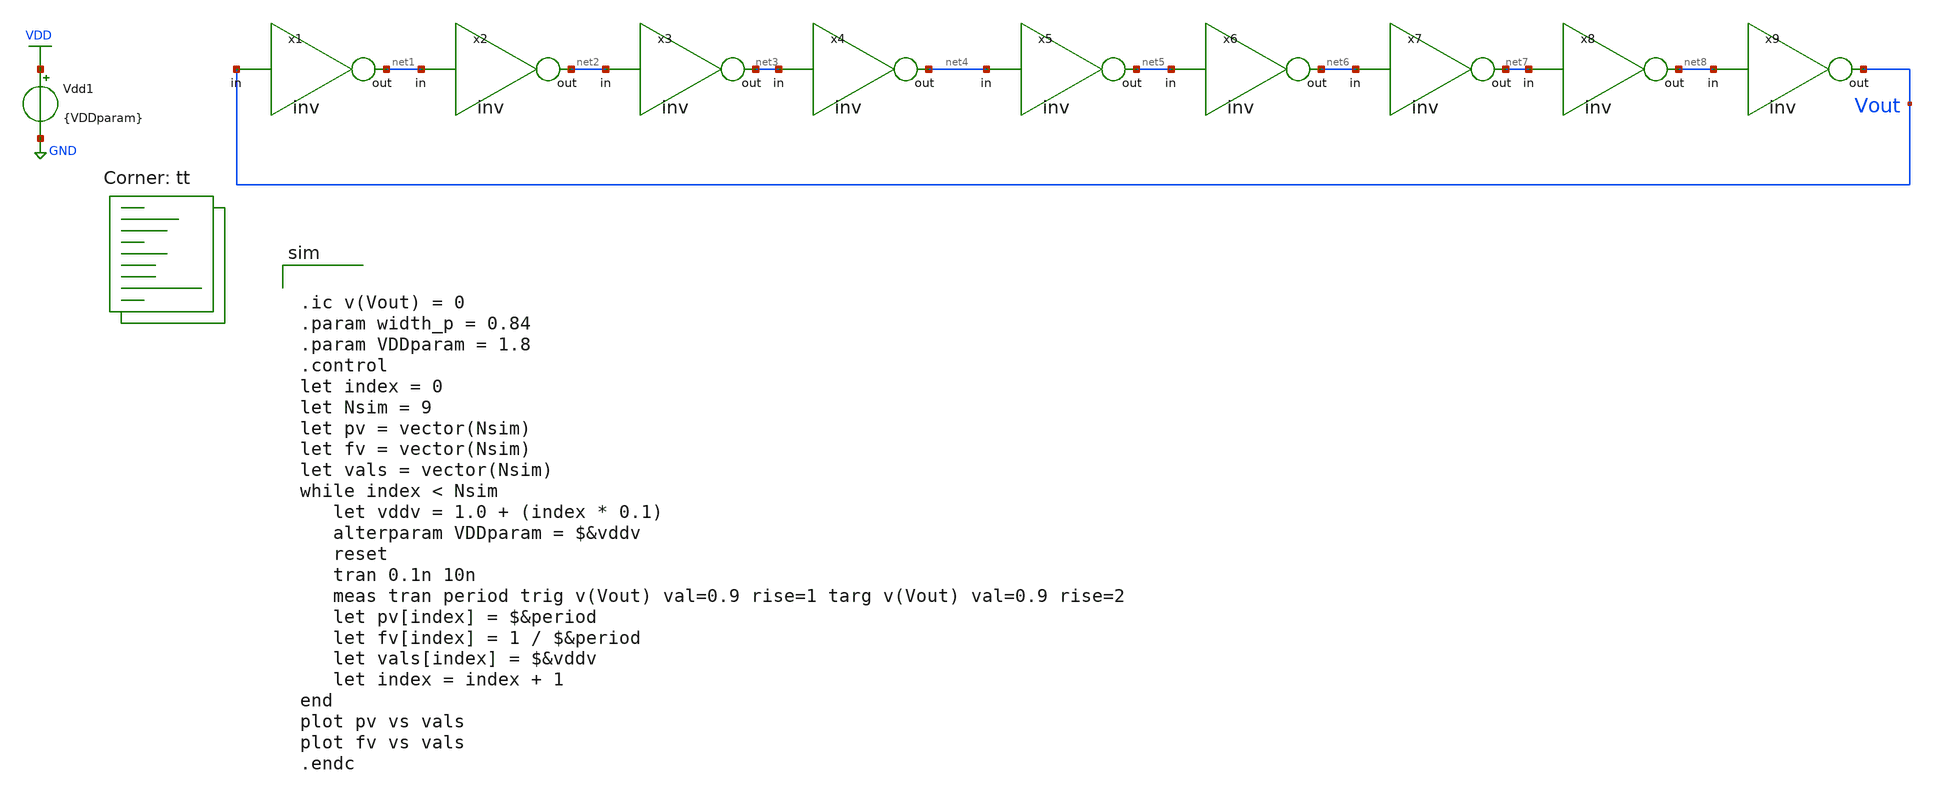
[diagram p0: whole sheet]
** sch_path: tutorial_4/tutorial_4_2c.sch
**.subckt tutorial_4_2c
x1 net1 Vout inv
x2 net2 net1 inv
x3 net3 net2 inv
x4 net4 net3 inv
x5 net5 net4 inv
x6 net6 net5 inv
x7 net7 net6 inv
Vdd1 VDD GND {VDDparam}
x8 net8 net7 inv
x9 Vout net8 inv
**** begin user architecture code


.ic v(Vout) = 0
.param width_p = 0.84
.param VDDparam = 1.8
.control
let index = 0
let Nsim = 9
let pv = vector(Nsim)
let fv = vector(Nsim)
let vals = vector(Nsim)
while index < Nsim
   let vddv = 1.0 + (index * 0.1)
   alterparam VDDparam = $&vddv
   reset
   tran 0.1n 10n
   meas tran period trig v(Vout) val=0.9 rise=1 targ v(Vout) val=0.9 rise=2
   let pv[index] = $&period
   let fv[index] = 1 / $&period
   let vals[index] = $&vddv
   let index = index + 1
end
plot pv vs vals
plot fv vs vals
.endc

.lib $::SKYWATER_MODELS/sky130.lib.spice tt
**** end user architecture code
**.ends

* expanding   symbol:  /home/EE23B038/ee5311/tutorial_4/inv.sym # of pins=2
** sym_path: tutorial_4/inv.sym
** sch_path: tutorial_4/inv.sch
.subckt inv out in
*.ipin in
*.opin out
XM1 out in GND GND sky130_fd_pr__nfet_01v8 L=0.15 W=0.42 nf=1 ad='int((nf+1)/2) * W/nf * 0.29' as='int((nf+2)/2) * W/nf * 0.29'
+ pd='2*int((nf+1)/2) * (W/nf + 0.29)' ps='2*int((nf+2)/2) * (W/nf + 0.29)' nrd='0.29 / W' nrs='0.29 / W'
+ sa=0 sb=0 sd=0 mult=1 m=1
XM2 out in VDD VDD sky130_fd_pr__pfet_01v8 L=0.15 W={width_p} nf=1 ad='int((nf+1)/2) * W/nf * 0.29' as='int((nf+2)/2) * W/nf * 0.29'
+ pd='2*int((nf+1)/2) * (W/nf + 0.29)' ps='2*int((nf+2)/2) * (W/nf + 0.29)' nrd='0.29 / W' nrs='0.29 / W'
+ sa=0 sb=0 sd=0 mult=1 m=1
.ends

.GLOBAL GND
.GLOBAL VDD
.end
